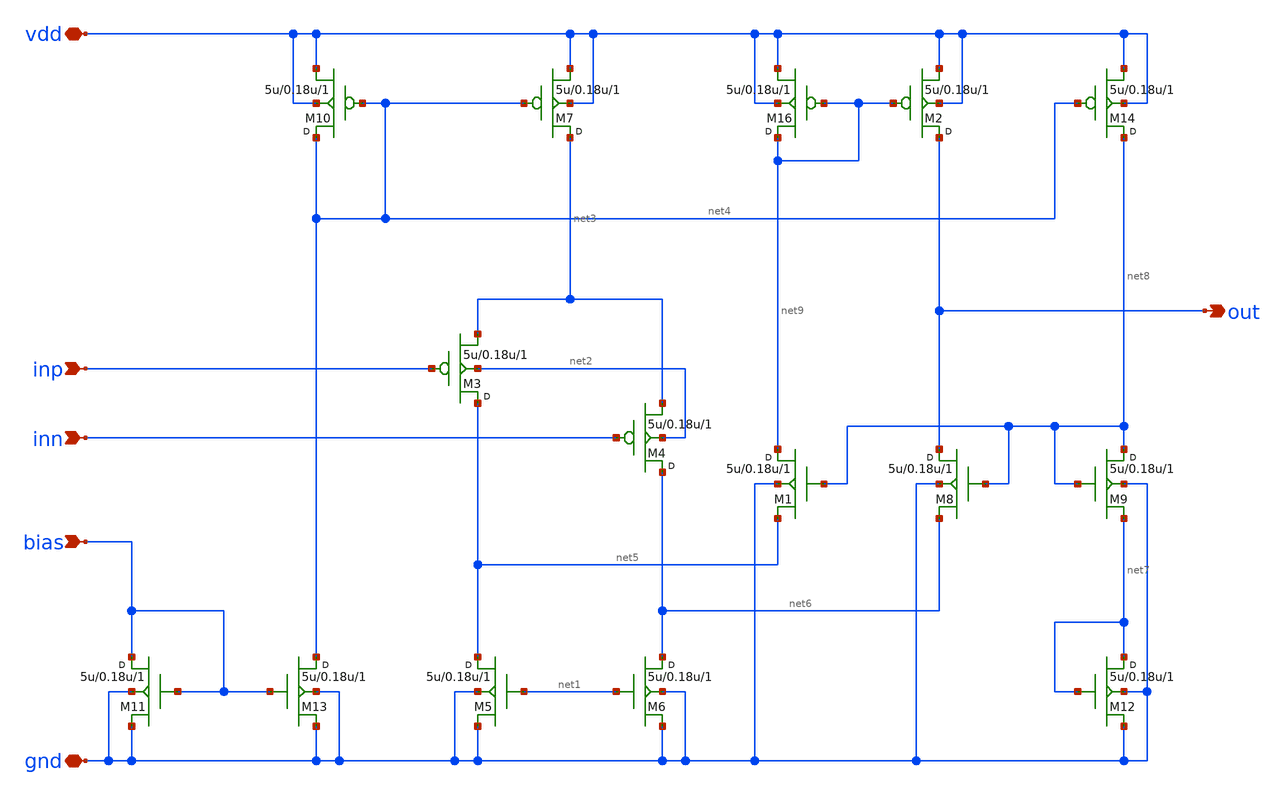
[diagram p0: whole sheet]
** sch_path: design/dac_cmfb_opamp/bandgap_opamp.sch
**.subckt bandgap_opamp inp inn bias out vdd gnd
*.ipin inp
*.ipin inn
*.ipin bias
*.opin out
*.iopin vdd
*.iopin gnd
M3 net5 inp net3 net2 pmos w=5u l=0.18u m=1
M4 net6 inn net3 net2 pmos w=5u l=0.18u m=1
M5 net5 net1 gnd gnd nmos w=5u l=0.18u m=1
M6 net6 net1 gnd gnd nmos w=5u l=0.18u m=1
M7 net3 net4 vdd vdd pmos w=5u l=0.18u m=1
M8 out net8 net6 gnd nmos w=5u l=0.18u m=1
M12 net7 net7 gnd gnd nmos w=5u l=0.18u m=1
M16 net9 net9 vdd vdd pmos w=5u l=0.18u m=1
M1 net9 net8 net5 gnd nmos w=5u l=0.18u m=1
M2 out net9 vdd vdd pmos w=5u l=0.18u m=1
M9 net8 net8 net7 gnd nmos w=5u l=0.18u m=1
M10 net4 net4 vdd vdd pmos w=5u l=0.18u m=1
M11 bias bias gnd gnd nmos w=5u l=0.18u m=1
M13 net4 bias gnd gnd nmos w=5u l=0.18u m=1
M14 net8 net4 vdd vdd pmos w=5u l=0.18u m=1
**.ends
.end
